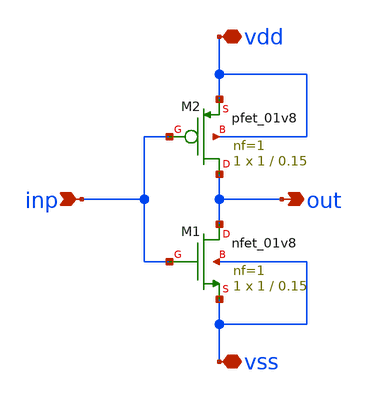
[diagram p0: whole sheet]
** sch_path: xschem/single_inverter.sch
**.subckt single_inverter vdd vss inp out
*.iopin vdd
*.iopin vss
*.ipin inp
*.opin out
XM1 out inp vss vss sky130_fd_pr__nfet_01v8 L=0.15 W=1 nf=1 ad='int((nf+1)/2) * W/nf * 0.29' as='int((nf+2)/2) * W/nf * 0.29'
+ pd='2*int((nf+1)/2) * (W/nf + 0.29)' ps='2*int((nf+2)/2) * (W/nf + 0.29)' nrd='0.29 / W' nrs='0.29 / W'
+ sa=0 sb=0 sd=0 mult=1 m=1
XM2 out inp vdd vdd sky130_fd_pr__pfet_01v8 L=0.15 W=1 nf=1 ad='int((nf+1)/2) * W/nf * 0.29' as='int((nf+2)/2) * W/nf * 0.29'
+ pd='2*int((nf+1)/2) * (W/nf + 0.29)' ps='2*int((nf+2)/2) * (W/nf + 0.29)' nrd='0.29 / W' nrs='0.29 / W'
+ sa=0 sb=0 sd=0 mult=1 m=1
**.ends
.end
